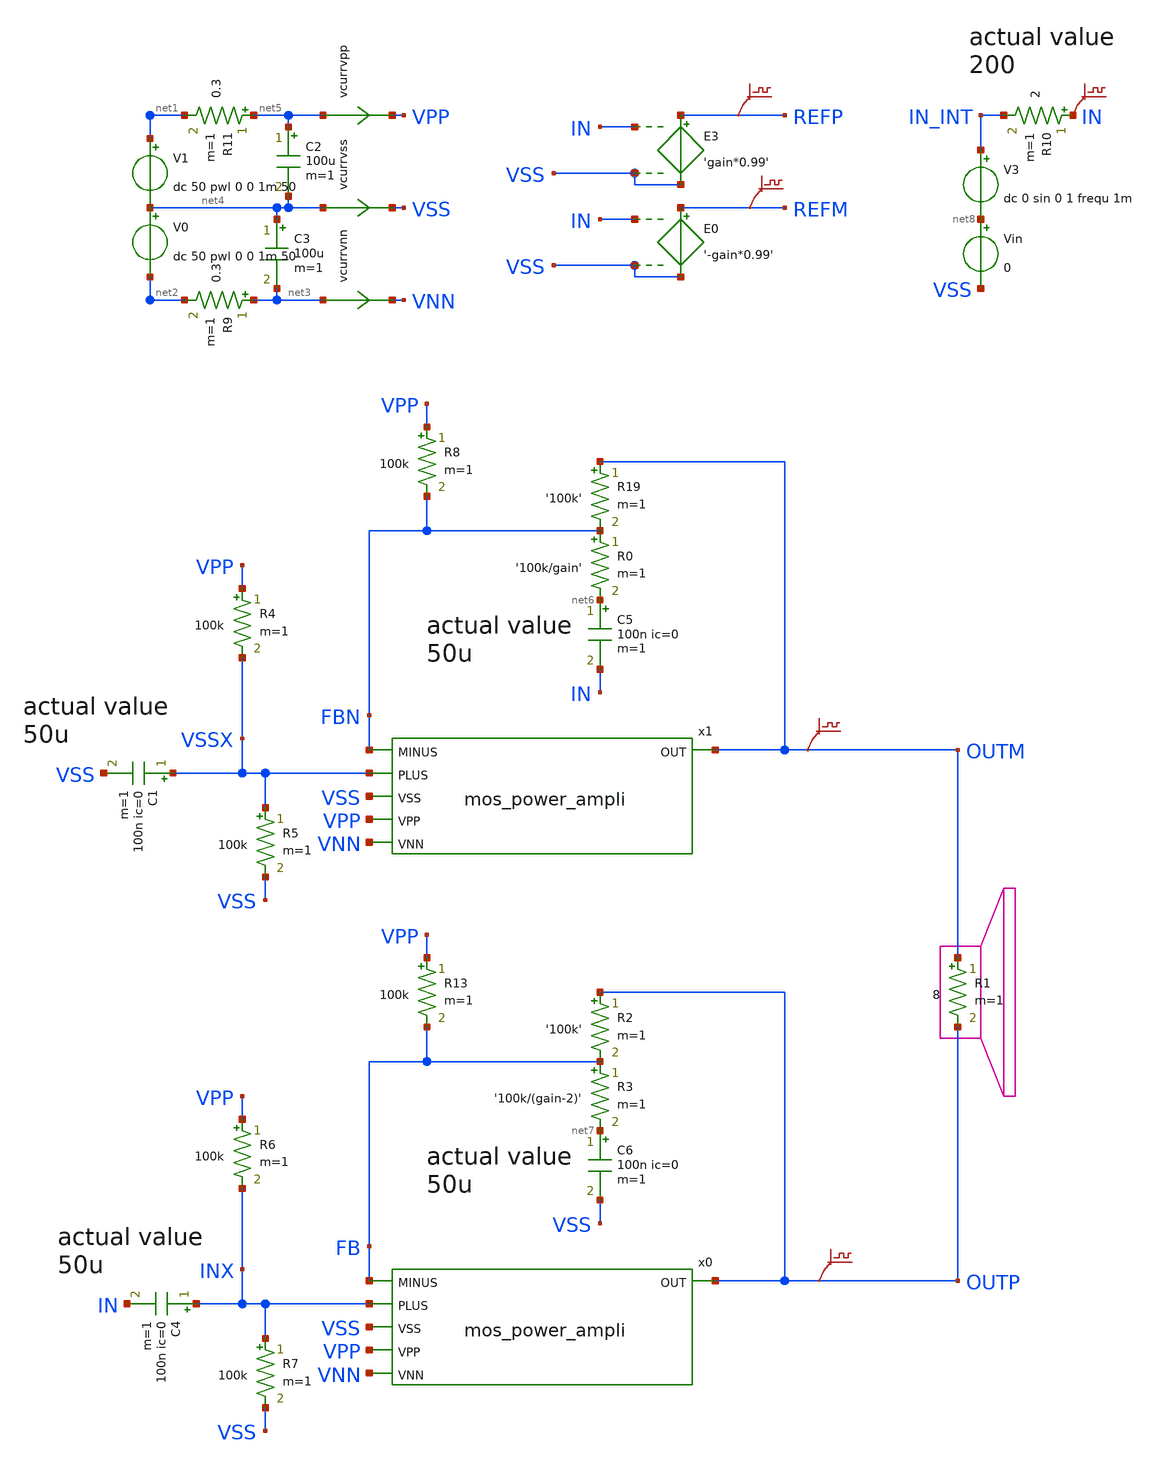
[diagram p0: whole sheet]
** sch_path: xschem_library/examples/poweramp.sch
**.subckt poweramp
V1 net1 net4 dc 50 pwl 0 0 1m 50
V0 net4 net2 dc 50 pwl 0 0 1m 50
R1 OUTM OUTP 8 m=1
E3 REFP VSS IN VSS 'gain*0.99'
C3 net4 net3 100u m=1
R11 net5 net1 0.3 m=1
R9 net3 net2 0.3 m=1
R19 OUTM FBN '100k' m=1
R0 FBN net6 '100k/gain' m=1
x1 FBN VSSX VSS OUTM VPP VNN mos_power_ampli
x0 FB INX VSS OUTP VPP VNN mos_power_ampli
R6 VPP INX 100k m=1
R7 INX VSS 100k m=1
E0 REFM VSS IN VSS '-gain*0.99'
C5 net6 IN 100n ic=0 m=1
C6 net7 VSS 100n ic=0 m=1
R2 OUTP FB '100k' m=1
R3 FB net7 '100k/(gain-2)' m=1
V3 IN_INT net8 dc 0 sin 0 1 frequ 1m
R4 VPP VSSX 100k m=1
R5 VSSX VSS 100k m=1
R8 VPP FBN 100k m=1
C4 INX IN 100n ic=0 m=1
C1 VSSX VSS 100n ic=0 m=1
R10 IN IN_INT 2 m=1
R13 VPP FB 100k m=1
Vin net8 VSS 0
vcurrvpp net5 VPP 0
.save i(vcurrvpp)
vcurrvnn net3 VNN 0
.save i(vcurrvnn)
vcurrvss net4 VSS 0
.save i(vcurrvss)
C2 net5 net4 100u m=1
.save v(outm)
.save v(outp)
.save v(refp)
.save v(refm)
.save v(in)
**** begin user architecture code

.option PARHIER=LOCAL RUNLVL=6 post MODMONTE=1 warn maxwarns=400
.option ITL4=20000 ITL5=0
* .option sampling_method = SRS
* .option method=gear
vvss vss 0 dc 0
.temp 30

.param frequ=5k
.param gain=45
.op
.tran  6e-7 0.06 uic


** models are generally not free: you must download
** SPICE models for active devices and put them  into the below
** referenced file in simulation directory.
.include "models_poweramp.txt"
* .save all
* .option savecurrents
* .FOUR 20k v(outm,outp)
* .probe i(*)
.save p(r*) p(v*)


**** end user architecture code
**.ends

* expanding   symbol:  mos_power_ampli.sym # of pins=6
** sym_path: xschem_library/examples/mos_power_ampli.sym
** sch_path: xschem_library/examples/mos_power_ampli.sch
.subckt mos_power_ampli MINUS PLUS VSS OUT VPP VNN
*.ipin PLUS
*.ipin VPP
*.ipin VNN
*.opin OUT
*.ipin MINUS
*.ipin VSS
xm2 net1 GB SB irf540 m=1
R7 GB SB 190 m=1
xm1 VPP GA SA irf540 m=1
R0 GA SA 190 m=1
R2 VPP E2 50 m=1
R3 VBOOST E1 50 m=1
Q5 C5 PLUS E9 q2n2222 area=1 m=1
Q4 net8 net2 E4 q2n2907p area=1 m=1
R9 VBOOST E4 50 m=1
Q6 C6 C2 net5 q2n2907p area=1 m=1
R4 VPP E6 50 m=1
vd OUTI net1 0
.save i(vd)
vu SA OUTI 0
.save i(vu)
Q1 net2 net2 E1 q2n2907p area=1 m=1
Q2 C2 C2 net4 q2n2907p area=1 m=1
Q9 C9 MINUS E9 q2n2222 area=1 m=1
R11 GB net6 1300 m=1
Q8 C8 VSS E8 q2n2907p area=1 m=1
C12 VBOOST net3 40u m=1
D0 VPP VBOOST d1n4148 area=1
R18 net3 OUTI 200 m=1
D1 VPP VBOOST d1n758
R14 B1 net7 4k m=1
Q11 GA B1 E11 q2n2907p area=1 m=1
R15 VBOOST B1 4k m=1
R5 E9 net9 120 m=1
R6 net9 net10 120 m=1
D2 VSS B3 d1n755
Q3 C3 B3 E3 q2n2222 area=1 m=1
R1 VPP B3 10k m=1
R10 E3 VSS 170 m=1
C3 B3 VSS 100n m=1
R12 C6 E8 1300 m=1
R13 C2 C9 300 m=1
Q7 C7 C9 C5 q2n2222 area=1 m=1
v0 SB VNN 0
.save i(v0)
v1 E6 net5 0
.save i(v1)
v2 E2 net4 0
.save i(v2)
v3 net10 C3 0
.save i(v3)
v4 C8 net6 0
.save i(v4)
v5 net7 OUTI 0
.save i(v5)
v6 net2 C7 0
.save i(v6)
v7 net8 E11 0
.save i(v7)
.save v(gb)
.save v(sb)
.save v(ga)
.save v(sa)
v8 OUTI OUT 0
.save i(v8)
.save v(ga)
.save v(gb)
.save v(c2)
.save v(net2)
.save v(c7)
.save v(test[3])
.save v(test[2])
.save v(test[1])
.save v(test[0])
R8[3] TEST[3] VSS 200 m=1
R8[2] TEST[2] VSS 200 m=1
R8[1] TEST[1] VSS 200 m=1
R8[0] TEST[0] VSS 200 m=1
.save v(vboost)
**** begin user architecture code

* .probe v(ga,sa) v(gb,sb)
* .probe p(q*) p(r*) i(r*) p(xm1) p(xm2) i(d*)
**** end user architecture code
.ends

.end
